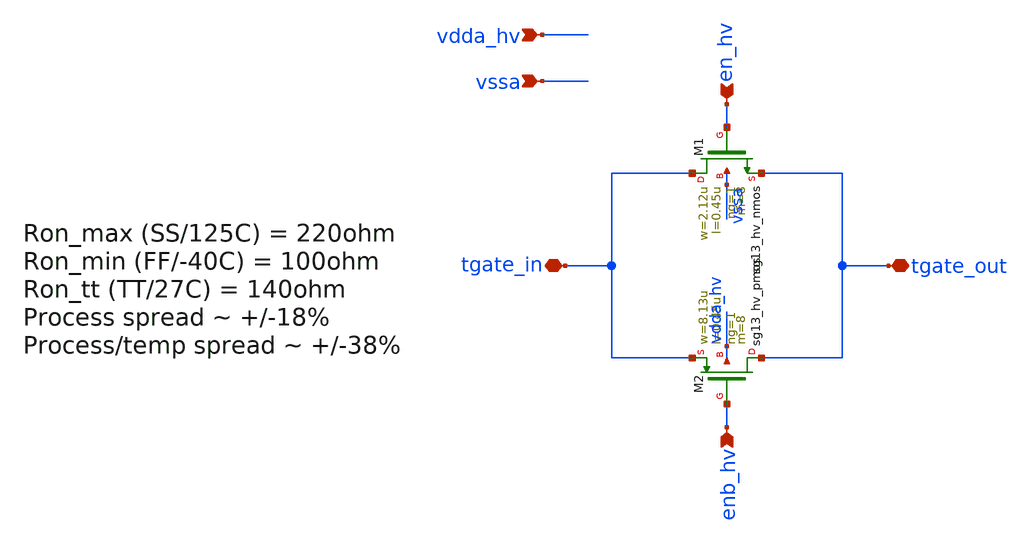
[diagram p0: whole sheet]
** sch_path: Schematics_Layout/sunrise_tgate/sunrise_tgate.sch
**.subckt sunrise_tgate vdda_hv vssa tgate_in tgate_out en_hv enb_hv
*.ipin vdda_hv
*.ipin vssa
*.iopin tgate_in
*.iopin tgate_out
*.ipin en_hv
*.ipin enb_hv
XM1 tgate_in en_hv tgate_out vssa sg13_hv_nmos w=2.12u l=0.45u ng=1 m=8 mm_ok=1
XM2 tgate_out enb_hv tgate_in vdda_hv sg13_hv_pmos w=8.13u l=0.45u ng=1 m=8 mm_ok=1
**.ends
.end
